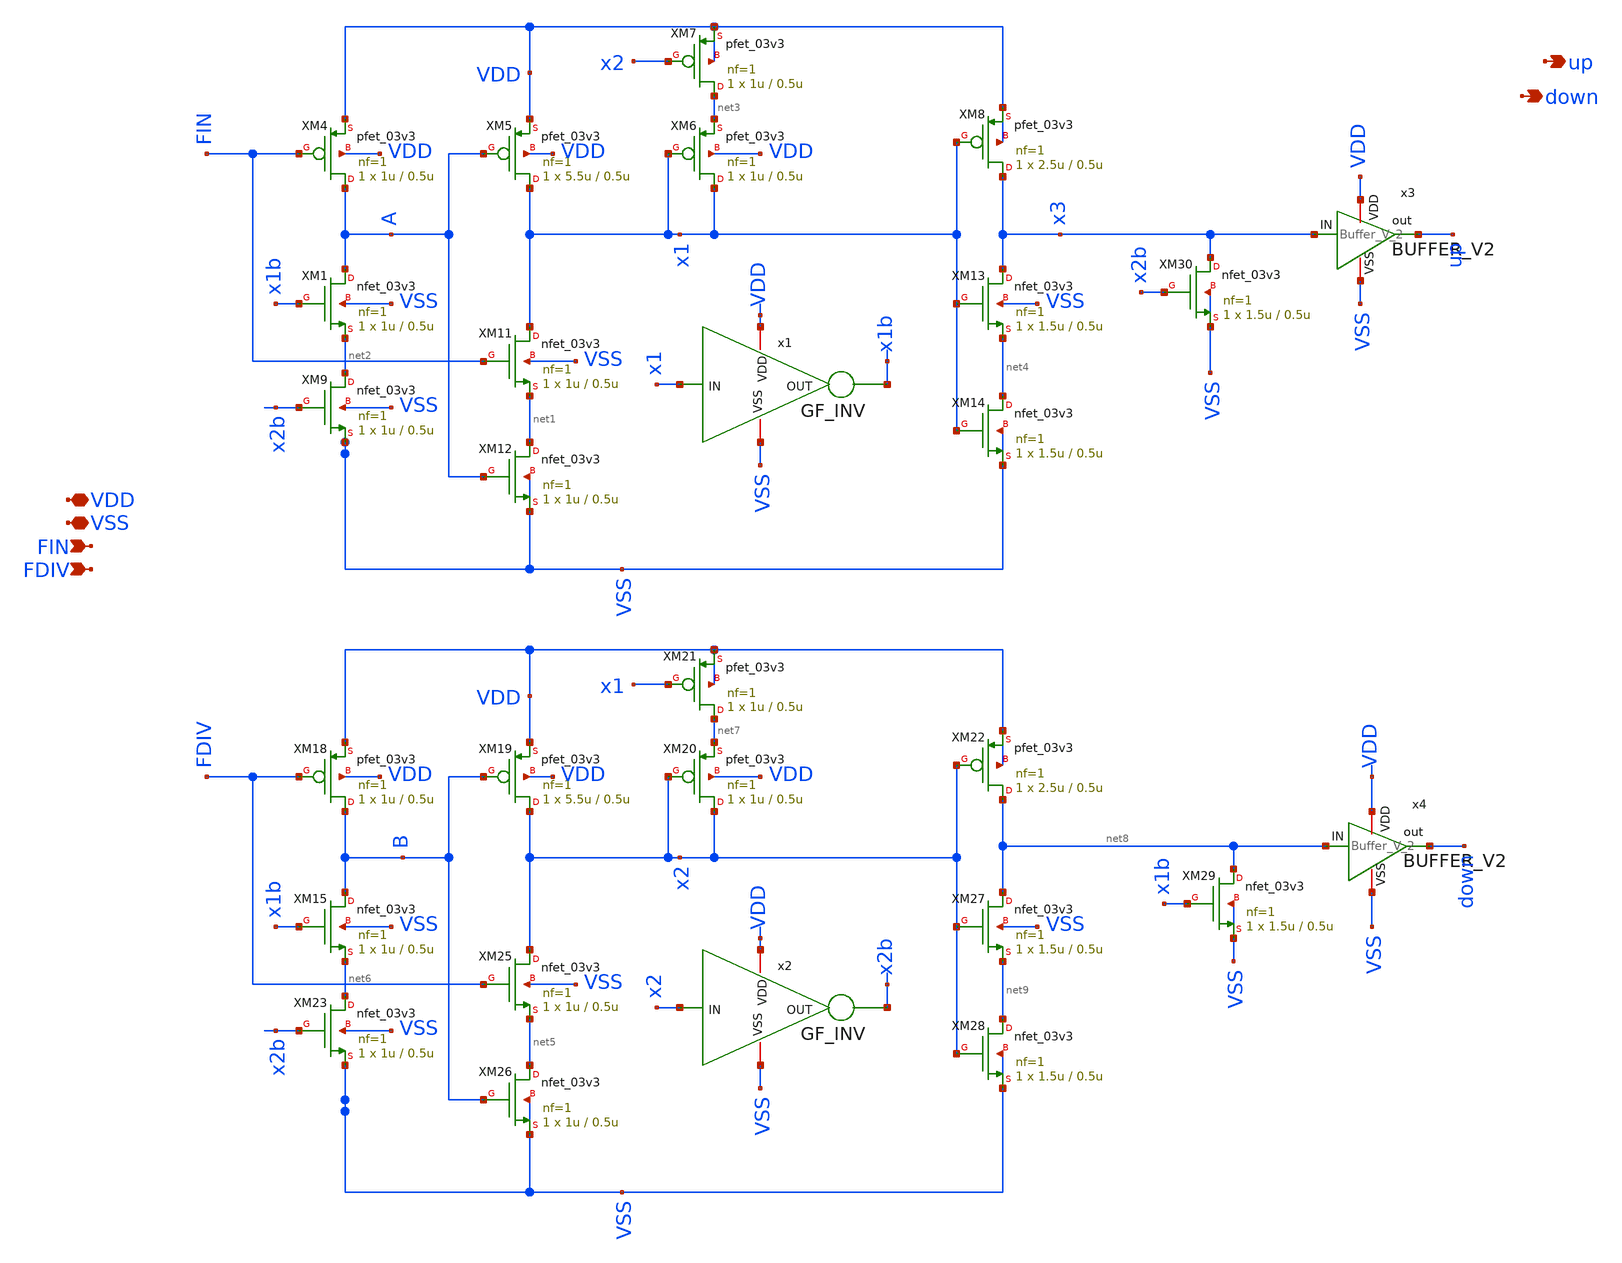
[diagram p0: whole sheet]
** sch_path: PLL-main/schematic/xschem/PFD_ver_2.sch
**.subckt PFD_ver_2 VDD VSS FIN FDIV up down
*.iopin VDD
*.iopin VSS
*.ipin FIN
*.ipin FDIV
*.opin up
*.opin down
XM1 A x1b net2 VSS nfet_03v3 L=0.5u W=1u nf=1 ad='int((nf+1)/2) * W/nf * 0.18u' as='int((nf+2)/2) * W/nf * 0.18u'
+ pd='2*int((nf+1)/2) * (W/nf + 0.18u)' ps='2*int((nf+2)/2) * (W/nf + 0.18u)' nrd='0.18u / W' nrs='0.18u / W'
+ sa=0 sb=0 sd=0 m=1
XM4 A FIN VDD VDD pfet_03v3 L=0.5u W=1u nf=1 ad='int((nf+1)/2) * W/nf * 0.18u' as='int((nf+2)/2) * W/nf * 0.18u'
+ pd='2*int((nf+1)/2) * (W/nf + 0.18u)' ps='2*int((nf+2)/2) * (W/nf + 0.18u)' nrd='0.18u / W' nrs='0.18u / W'
+ sa=0 sb=0 sd=0 m=1
XM5 x1 A VDD VDD pfet_03v3 L=0.5u W=5.5u nf=1 ad='int((nf+1)/2) * W/nf * 0.18u' as='int((nf+2)/2) * W/nf * 0.18u'
+ pd='2*int((nf+1)/2) * (W/nf + 0.18u)' ps='2*int((nf+2)/2) * (W/nf + 0.18u)' nrd='0.18u / W' nrs='0.18u / W'
+ sa=0 sb=0 sd=0 m=1
XM6 x1 x1 net3 VDD pfet_03v3 L=0.5u W=1u nf=1 ad='int((nf+1)/2) * W/nf * 0.18u' as='int((nf+2)/2) * W/nf * 0.18u'
+ pd='2*int((nf+1)/2) * (W/nf + 0.18u)' ps='2*int((nf+2)/2) * (W/nf + 0.18u)' nrd='0.18u / W' nrs='0.18u / W'
+ sa=0 sb=0 sd=0 m=1
XM7 net3 x2 VDD VDD pfet_03v3 L=0.5u W=1u nf=1 ad='int((nf+1)/2) * W/nf * 0.18u' as='int((nf+2)/2) * W/nf * 0.18u'
+ pd='2*int((nf+1)/2) * (W/nf + 0.18u)' ps='2*int((nf+2)/2) * (W/nf + 0.18u)' nrd='0.18u / W' nrs='0.18u / W'
+ sa=0 sb=0 sd=0 m=1
XM8 x3 x1 VDD VDD pfet_03v3 L=0.5u W=2.5u nf=1 ad='int((nf+1)/2) * W/nf * 0.18u' as='int((nf+2)/2) * W/nf * 0.18u'
+ pd='2*int((nf+1)/2) * (W/nf + 0.18u)' ps='2*int((nf+2)/2) * (W/nf + 0.18u)' nrd='0.18u / W' nrs='0.18u / W'
+ sa=0 sb=0 sd=0 m=1
XM9 net2 x2b VSS VSS nfet_03v3 L=0.5u W=1u nf=1 ad='int((nf+1)/2) * W/nf * 0.18u' as='int((nf+2)/2) * W/nf * 0.18u'
+ pd='2*int((nf+1)/2) * (W/nf + 0.18u)' ps='2*int((nf+2)/2) * (W/nf + 0.18u)' nrd='0.18u / W' nrs='0.18u / W'
+ sa=0 sb=0 sd=0 m=1
XM11 x1 FIN net1 VSS nfet_03v3 L=0.5u W=1u nf=1 ad='int((nf+1)/2) * W/nf * 0.18u' as='int((nf+2)/2) * W/nf * 0.18u'
+ pd='2*int((nf+1)/2) * (W/nf + 0.18u)' ps='2*int((nf+2)/2) * (W/nf + 0.18u)' nrd='0.18u / W' nrs='0.18u / W'
+ sa=0 sb=0 sd=0 m=1
XM12 net1 A VSS VSS nfet_03v3 L=0.5u W=1u nf=1 ad='int((nf+1)/2) * W/nf * 0.18u' as='int((nf+2)/2) * W/nf * 0.18u'
+ pd='2*int((nf+1)/2) * (W/nf + 0.18u)' ps='2*int((nf+2)/2) * (W/nf + 0.18u)' nrd='0.18u / W' nrs='0.18u / W'
+ sa=0 sb=0 sd=0 m=1
XM13 x3 x1 net4 VSS nfet_03v3 L=0.5u W=1.5u nf=1 ad='int((nf+1)/2) * W/nf * 0.18u' as='int((nf+2)/2) * W/nf * 0.18u'
+ pd='2*int((nf+1)/2) * (W/nf + 0.18u)' ps='2*int((nf+2)/2) * (W/nf + 0.18u)' nrd='0.18u / W' nrs='0.18u / W'
+ sa=0 sb=0 sd=0 m=1
XM14 net4 x1 VSS VSS nfet_03v3 L=0.5u W=1.5u nf=1 ad='int((nf+1)/2) * W/nf * 0.18u' as='int((nf+2)/2) * W/nf * 0.18u'
+ pd='2*int((nf+1)/2) * (W/nf + 0.18u)' ps='2*int((nf+2)/2) * (W/nf + 0.18u)' nrd='0.18u / W' nrs='0.18u / W'
+ sa=0 sb=0 sd=0 m=1
x1 VSS VDD x1b x1 GF_INV
XM15 B x1b net6 VSS nfet_03v3 L=0.5u W=1u nf=1 ad='int((nf+1)/2) * W/nf * 0.18u' as='int((nf+2)/2) * W/nf * 0.18u'
+ pd='2*int((nf+1)/2) * (W/nf + 0.18u)' ps='2*int((nf+2)/2) * (W/nf + 0.18u)' nrd='0.18u / W' nrs='0.18u / W'
+ sa=0 sb=0 sd=0 m=1
XM18 B FDIV VDD VDD pfet_03v3 L=0.5u W=1u nf=1 ad='int((nf+1)/2) * W/nf * 0.18u' as='int((nf+2)/2) * W/nf * 0.18u'
+ pd='2*int((nf+1)/2) * (W/nf + 0.18u)' ps='2*int((nf+2)/2) * (W/nf + 0.18u)' nrd='0.18u / W' nrs='0.18u / W'
+ sa=0 sb=0 sd=0 m=1
XM19 x2 B VDD VDD pfet_03v3 L=0.5u W=5.5u nf=1 ad='int((nf+1)/2) * W/nf * 0.18u' as='int((nf+2)/2) * W/nf * 0.18u'
+ pd='2*int((nf+1)/2) * (W/nf + 0.18u)' ps='2*int((nf+2)/2) * (W/nf + 0.18u)' nrd='0.18u / W' nrs='0.18u / W'
+ sa=0 sb=0 sd=0 m=1
XM20 x2 x2 net7 VDD pfet_03v3 L=0.5u W=1u nf=1 ad='int((nf+1)/2) * W/nf * 0.18u' as='int((nf+2)/2) * W/nf * 0.18u'
+ pd='2*int((nf+1)/2) * (W/nf + 0.18u)' ps='2*int((nf+2)/2) * (W/nf + 0.18u)' nrd='0.18u / W' nrs='0.18u / W'
+ sa=0 sb=0 sd=0 m=1
XM21 net7 x1 VDD VDD pfet_03v3 L=0.5u W=1u nf=1 ad='int((nf+1)/2) * W/nf * 0.18u' as='int((nf+2)/2) * W/nf * 0.18u'
+ pd='2*int((nf+1)/2) * (W/nf + 0.18u)' ps='2*int((nf+2)/2) * (W/nf + 0.18u)' nrd='0.18u / W' nrs='0.18u / W'
+ sa=0 sb=0 sd=0 m=1
XM22 net8 x2 VDD VDD pfet_03v3 L=0.5u W=2.5u nf=1 ad='int((nf+1)/2) * W/nf * 0.18u' as='int((nf+2)/2) * W/nf * 0.18u'
+ pd='2*int((nf+1)/2) * (W/nf + 0.18u)' ps='2*int((nf+2)/2) * (W/nf + 0.18u)' nrd='0.18u / W' nrs='0.18u / W'
+ sa=0 sb=0 sd=0 m=1
XM23 net6 x2b VSS VSS nfet_03v3 L=0.5u W=1u nf=1 ad='int((nf+1)/2) * W/nf * 0.18u' as='int((nf+2)/2) * W/nf * 0.18u'
+ pd='2*int((nf+1)/2) * (W/nf + 0.18u)' ps='2*int((nf+2)/2) * (W/nf + 0.18u)' nrd='0.18u / W' nrs='0.18u / W'
+ sa=0 sb=0 sd=0 m=1
XM25 x2 FDIV net5 VSS nfet_03v3 L=0.5u W=1u nf=1 ad='int((nf+1)/2) * W/nf * 0.18u' as='int((nf+2)/2) * W/nf * 0.18u'
+ pd='2*int((nf+1)/2) * (W/nf + 0.18u)' ps='2*int((nf+2)/2) * (W/nf + 0.18u)' nrd='0.18u / W' nrs='0.18u / W'
+ sa=0 sb=0 sd=0 m=1
XM26 net5 B VSS VSS nfet_03v3 L=0.5u W=1u nf=1 ad='int((nf+1)/2) * W/nf * 0.18u' as='int((nf+2)/2) * W/nf * 0.18u'
+ pd='2*int((nf+1)/2) * (W/nf + 0.18u)' ps='2*int((nf+2)/2) * (W/nf + 0.18u)' nrd='0.18u / W' nrs='0.18u / W'
+ sa=0 sb=0 sd=0 m=1
XM27 net8 x2 net9 VSS nfet_03v3 L=0.5u W=1.5u nf=1 ad='int((nf+1)/2) * W/nf * 0.18u' as='int((nf+2)/2) * W/nf * 0.18u'
+ pd='2*int((nf+1)/2) * (W/nf + 0.18u)' ps='2*int((nf+2)/2) * (W/nf + 0.18u)' nrd='0.18u / W' nrs='0.18u / W'
+ sa=0 sb=0 sd=0 m=1
XM28 net9 x2 VSS VSS nfet_03v3 L=0.5u W=1.5u nf=1 ad='int((nf+1)/2) * W/nf * 0.18u' as='int((nf+2)/2) * W/nf * 0.18u'
+ pd='2*int((nf+1)/2) * (W/nf + 0.18u)' ps='2*int((nf+2)/2) * (W/nf + 0.18u)' nrd='0.18u / W' nrs='0.18u / W'
+ sa=0 sb=0 sd=0 m=1
x2 VSS VDD x2b x2 GF_INV
XM29 net8 x1b VSS VSS nfet_03v3 L=0.5u W=1.5u nf=1 ad='int((nf+1)/2) * W/nf * 0.18u' as='int((nf+2)/2) * W/nf * 0.18u'
+ pd='2*int((nf+1)/2) * (W/nf + 0.18u)' ps='2*int((nf+2)/2) * (W/nf + 0.18u)' nrd='0.18u / W' nrs='0.18u / W'
+ sa=0 sb=0 sd=0 m=1
XM30 x3 x2b VSS VSS nfet_03v3 L=0.5u W=1.5u nf=1 ad='int((nf+1)/2) * W/nf * 0.18u' as='int((nf+2)/2) * W/nf * 0.18u'
+ pd='2*int((nf+1)/2) * (W/nf + 0.18u)' ps='2*int((nf+2)/2) * (W/nf + 0.18u)' nrd='0.18u / W' nrs='0.18u / W'
+ sa=0 sb=0 sd=0 m=1
x3 VDD x3 up VSS Buffer_V_2
x4 VDD net8 down VSS Buffer_V_2
**.ends
.end
